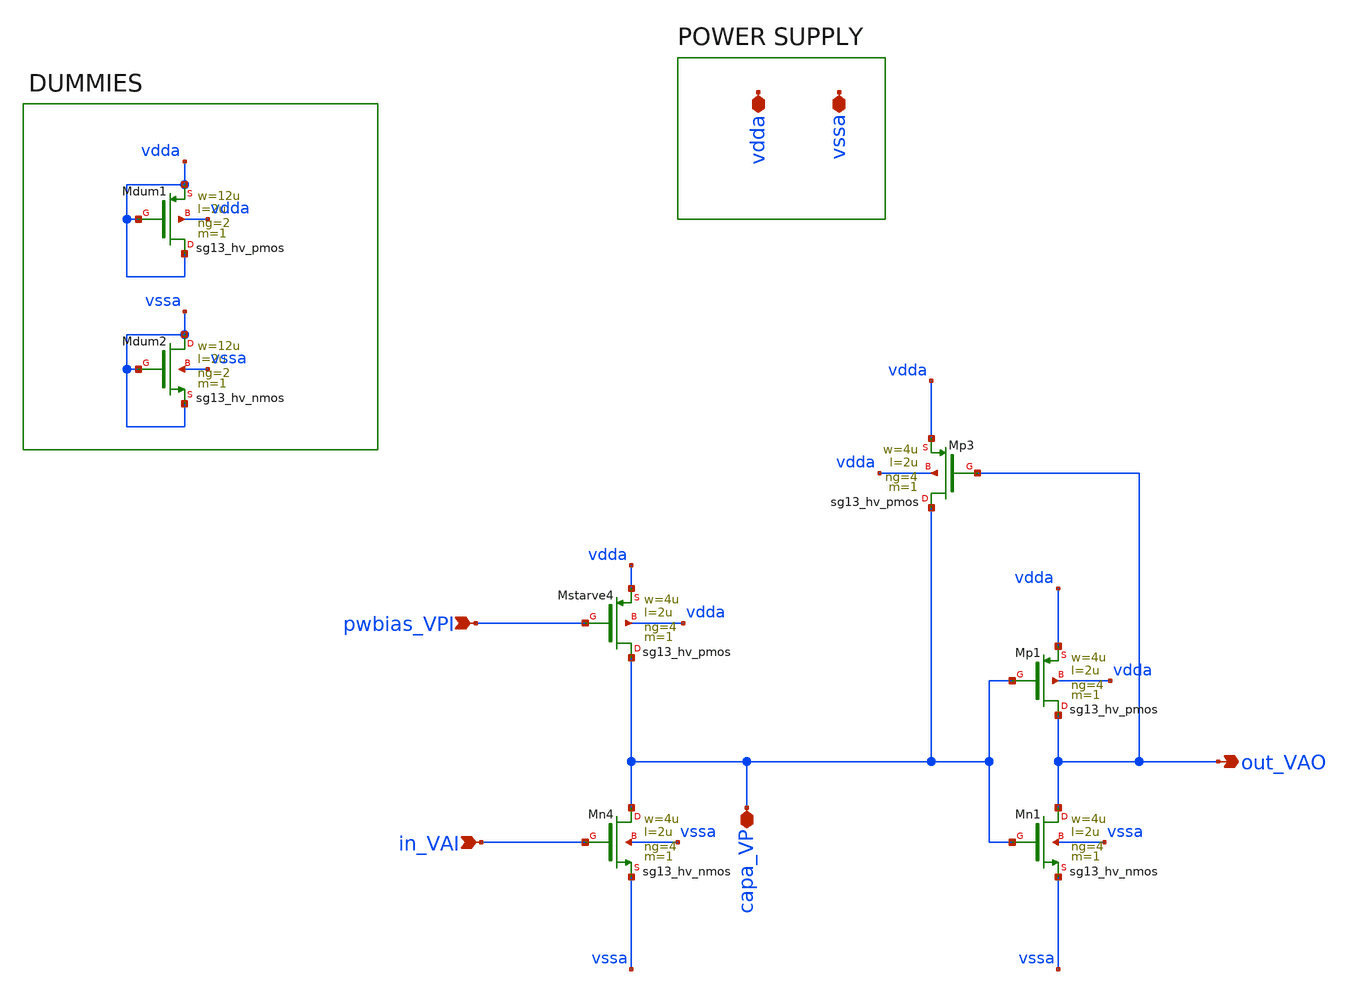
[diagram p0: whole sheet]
** sch_path: pulse_extender_V2.sch
**.subckt pulse_extender_V2 out_VAO pwbias_VPI in_VAI capa_VP vssa vdda
*.opin out_VAO
*.ipin pwbias_VPI
*.ipin in_VAI
*.iopin capa_VP
*.iopin vssa
*.iopin vdda
XMp1 out_VAO capa_VP vdda vdda sg13_hv_pmos w=4u l=2u ng=4 m=1 mm_ok=1
XMn1 out_VAO capa_VP vssa vssa sg13_hv_nmos w=4u l=2u ng=4 m=1 mm_ok=1
XMn4 capa_VP in_VAI vssa vssa sg13_hv_nmos w=4u l=2u ng=4 m=1 mm_ok=1
XMstarve4 capa_VP pwbias_VPI vdda vdda sg13_hv_pmos w=4u l=2u ng=4 m=1 mm_ok=1
XMp3 capa_VP out_VAO vdda vdda sg13_hv_pmos w=4u l=2u ng=4 m=1 mm_ok=1
XMdum2 vssa vssa vssa vssa sg13_hv_nmos w=12u l=2u ng=2 m=1 mm_ok=1
XMdum1 vdda vdda vdda vdda sg13_hv_pmos w=12u l=2u ng=2 m=1 mm_ok=1
**.ends
.end
